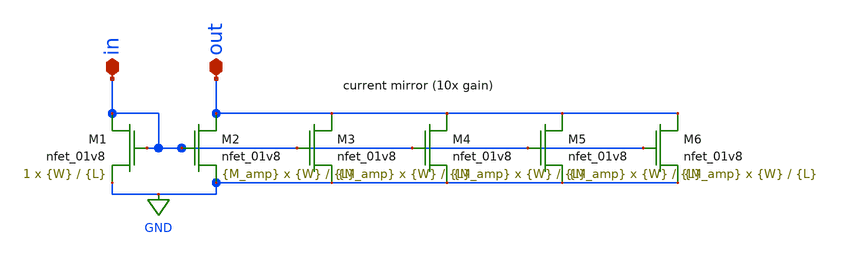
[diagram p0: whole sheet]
** sch_path: schemas/gain_mirror.sch
**.subckt gain_mirror in out
*.iopin in
*.iopin out
XM1 in in GND GND sky130_fd_pr__nfet_01v8 L={L} W={W} nf=1 ad='int((nf+1)/2) * W/nf * 0.29' as='int((nf+2)/2) * W/nf * 0.29'
+ pd='2*int((nf+1)/2) * (W/nf + 0.29)' ps='2*int((nf+2)/2) * (W/nf + 0.29)' nrd='0.29 / W' nrs='0.29 / W'
+ sa=0 sb=0 sd=0 mult=1 m=1
XM2 out in GND GND sky130_fd_pr__nfet_01v8 L={L} W={W} nf=1 ad='int((nf+1)/2) * W/nf * 0.29' as='int((nf+2)/2) * W/nf * 0.29'
+ pd='2*int((nf+1)/2) * (W/nf + 0.29)' ps='2*int((nf+2)/2) * (W/nf + 0.29)' nrd='0.29 / W' nrs='0.29 / W'
+ sa=0 sb=0 sd=0 mult={M_amp} m={M_amp}
XM3 out in GND GND sky130_fd_pr__nfet_01v8 L={L} W={W} nf=1 ad='int((nf+1)/2) * W/nf * 0.29' as='int((nf+2)/2) * W/nf * 0.29'
+ pd='2*int((nf+1)/2) * (W/nf + 0.29)' ps='2*int((nf+2)/2) * (W/nf + 0.29)' nrd='0.29 / W' nrs='0.29 / W'
+ sa=0 sb=0 sd=0 mult={M_amp} m={M_amp}
XM4 out in GND GND sky130_fd_pr__nfet_01v8 L={L} W={W} nf=1 ad='int((nf+1)/2) * W/nf * 0.29' as='int((nf+2)/2) * W/nf * 0.29'
+ pd='2*int((nf+1)/2) * (W/nf + 0.29)' ps='2*int((nf+2)/2) * (W/nf + 0.29)' nrd='0.29 / W' nrs='0.29 / W'
+ sa=0 sb=0 sd=0 mult={M_amp} m={M_amp}
XM5 out in GND GND sky130_fd_pr__nfet_01v8 L={L} W={W} nf=1 ad='int((nf+1)/2) * W/nf * 0.29' as='int((nf+2)/2) * W/nf * 0.29'
+ pd='2*int((nf+1)/2) * (W/nf + 0.29)' ps='2*int((nf+2)/2) * (W/nf + 0.29)' nrd='0.29 / W' nrs='0.29 / W'
+ sa=0 sb=0 sd=0 mult={M_amp} m={M_amp}
XM6 out in GND GND sky130_fd_pr__nfet_01v8 L={L} W={W} nf=1 ad='int((nf+1)/2) * W/nf * 0.29' as='int((nf+2)/2) * W/nf * 0.29'
+ pd='2*int((nf+1)/2) * (W/nf + 0.29)' ps='2*int((nf+2)/2) * (W/nf + 0.29)' nrd='0.29 / W' nrs='0.29 / W'
+ sa=0 sb=0 sd=0 mult={M_amp} m={M_amp}
**.ends
.GLOBAL GND
.end
